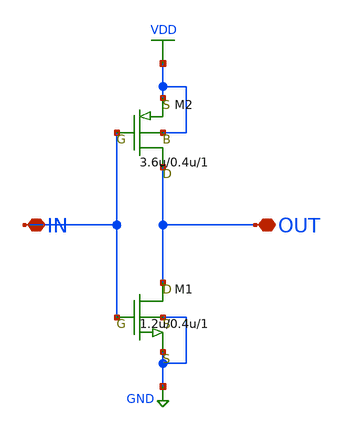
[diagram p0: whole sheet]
** sch_path: LR_hasegawa/LR_Work2/Citizen035/INVERTER_Citizen.sch
**.subckt INVERTER_Citizen OUT IN
*.iopin OUT
*.iopin IN
M1 OUT IN GND GND nch w=1.2u l=0.4u as=0 ps=0 ad=0 pd=0 m=1
M2 OUT IN VDD VDD pch w=3.6u l=0.4u as=0 ps=0 ad=0 pd=0 m=1
**.ends
.GLOBAL VDD
.GLOBAL GND
.end
